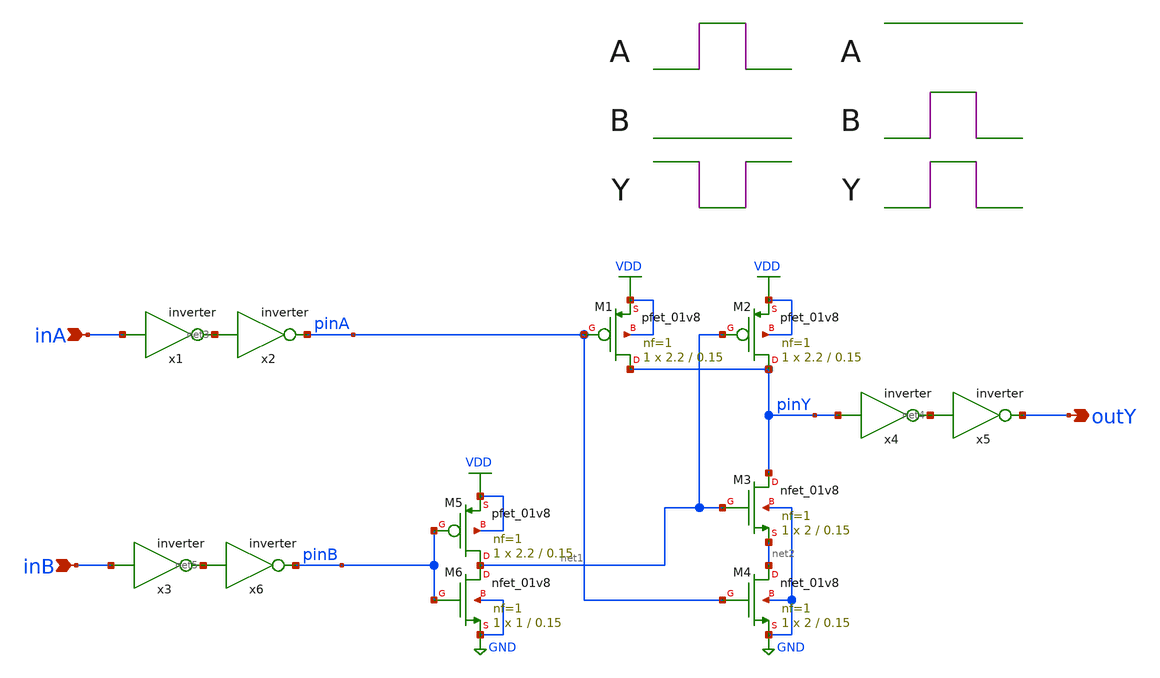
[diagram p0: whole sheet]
** sch_path: nandb_delay.sch
**.subckt nandb_delay inA outY inB
*.ipin inA
*.opin outY
*.ipin inB
x1 net3 inA inverter
x2 pinA net3 inverter
x4 net4 pinY inverter
x5 outY net4 inverter
x3 net5 inB inverter
x6 pinB net5 inverter
XM1 pinY pinA VDD VDD sky130_fd_pr__pfet_01v8 L=0.15 W=2.2 nf=1 ad='int((nf+1)/2) * W/nf * 0.29' as='int((nf+2)/2) * W/nf * 0.29'
+ pd='2*int((nf+1)/2) * (W/nf + 0.29)' ps='2*int((nf+2)/2) * (W/nf + 0.29)' nrd='0.29 / W' nrs='0.29 / W'
+ sa=0 sb=0 sd=0 mult=1 m=1
XM2 pinY net1 VDD VDD sky130_fd_pr__pfet_01v8 L=0.15 W=2.2 nf=1 ad='int((nf+1)/2) * W/nf * 0.29' as='int((nf+2)/2) * W/nf * 0.29'
+ pd='2*int((nf+1)/2) * (W/nf + 0.29)' ps='2*int((nf+2)/2) * (W/nf + 0.29)' nrd='0.29 / W' nrs='0.29 / W'
+ sa=0 sb=0 sd=0 mult=1 m=1
XM3 pinY net1 net2 GND sky130_fd_pr__nfet_01v8 L=0.15 W=2 nf=1 ad='int((nf+1)/2) * W/nf * 0.29' as='int((nf+2)/2) * W/nf * 0.29'
+ pd='2*int((nf+1)/2) * (W/nf + 0.29)' ps='2*int((nf+2)/2) * (W/nf + 0.29)' nrd='0.29 / W' nrs='0.29 / W'
+ sa=0 sb=0 sd=0 mult=1 m=1
XM4 net2 pinA GND GND sky130_fd_pr__nfet_01v8 L=0.15 W=2 nf=1 ad='int((nf+1)/2) * W/nf * 0.29' as='int((nf+2)/2) * W/nf * 0.29'
+ pd='2*int((nf+1)/2) * (W/nf + 0.29)' ps='2*int((nf+2)/2) * (W/nf + 0.29)' nrd='0.29 / W' nrs='0.29 / W'
+ sa=0 sb=0 sd=0 mult=1 m=1
XM5 net1 pinB VDD VDD sky130_fd_pr__pfet_01v8 L=0.15 W=2.2 nf=1 ad='int((nf+1)/2) * W/nf * 0.29' as='int((nf+2)/2) * W/nf * 0.29'
+ pd='2*int((nf+1)/2) * (W/nf + 0.29)' ps='2*int((nf+2)/2) * (W/nf + 0.29)' nrd='0.29 / W' nrs='0.29 / W'
+ sa=0 sb=0 sd=0 mult=1 m=1
XM6 net1 pinB GND GND sky130_fd_pr__nfet_01v8 L=0.15 W=1 nf=1 ad='int((nf+1)/2) * W/nf * 0.29' as='int((nf+2)/2) * W/nf * 0.29'
+ pd='2*int((nf+1)/2) * (W/nf + 0.29)' ps='2*int((nf+2)/2) * (W/nf + 0.29)' nrd='0.29 / W' nrs='0.29 / W'
+ sa=0 sb=0 sd=0 mult=1 m=1
**** begin user architecture code


VA inA 0 dc 0
VB inB 0 dc 0
VD VDD 0 dc 1.8
.control
alter @va[PULSE] [ 0 1.8 1n 40p 40p 1n 3n ]
alter @vb[PULSE] [ 0 0 1n 40p 40p 1n 3n ]
tran 10p 3n
meas tran  in1 FIND time WHEN v(pina)=0.9 RISE=1 > NUL
meas tran out1 FIND time WHEN v(piny)=0.9 FALL=1 > NUL
meas tran  in2 FIND time WHEN v(pina)=0.9 FALL=1 > NUL
meas tran out2 FIND time WHEN v(piny)=0.9 RISE=1 > NUL

let calc1 = out1 - in1
set delaynab1 = $&calc1
let calc2 = out2 - in2
set delaynab2 = $&calc2

alter @vb[PULSE] [ 0 1.8 1n 40p 40p 1n 3n ]
alter @va[PULSE] [ 1.8 1.8 1n 40p 40p 1n 3n ]
tran 10p 3n
meas tran  in5 FIND time WHEN v(pinb)=0.9 RISE=1 > NUL
meas tran out5 FIND time WHEN v(piny)=0.9 RISE=1 > NUL
meas tran  in6 FIND time WHEN v(pinb)=0.9 FALL=1 > NUL
meas tran out6 FIND time WHEN v(piny)=0.9 FALL=1 > NUL

let calc5 = out5 - in5
set delaynab5 = $&calc5
let calc6 = out6 - in6
set delaynab6 = $&calc6

let calc5 = out5 - in5
set delayna5 = $&calc5
let calc6 = out6 - in6
set delayna6 = $&calc6

echo '*** NANDB DELAY CASE 1 ***'
echo 'A(LH) when B(H) ='{$delaynab1}
echo 'A(HL) when B(H) ='{$delaynab2}

echo '*** NANDB DELAY CASE 2 ***'
echo 'B(LH) when A(H) ='{$delaynab5}
echo 'B(HL) when A(H) ='{$delaynab6}

.endc


** opencircuitdesign pdks install
.lib $::SKYWATER_MODELS/sky130.lib.spice tt


**** end user architecture code
**.ends

* expanding   symbol:  inverter.sym # of pins=2
** sym_path: inverter.sym
** sch_path: inverter.sch
.subckt inverter Y A
*.ipin A
*.opin Y
XM1 Y A VDD VDD sky130_fd_pr__pfet_01v8 L=0.15 W=2.2 nf=1 ad='int((nf+1)/2) * W/nf * 0.29' as='int((nf+2)/2) * W/nf * 0.29'
+ pd='2*int((nf+1)/2) * (W/nf + 0.29)' ps='2*int((nf+2)/2) * (W/nf + 0.29)' nrd='0.29 / W' nrs='0.29 / W'
+ sa=0 sb=0 sd=0 mult=1 m=1
XM2 Y A GND GND sky130_fd_pr__nfet_01v8 L=0.15 W=1 nf=1 ad='int((nf+1)/2) * W/nf * 0.29' as='int((nf+2)/2) * W/nf * 0.29'
+ pd='2*int((nf+1)/2) * (W/nf + 0.29)' ps='2*int((nf+2)/2) * (W/nf + 0.29)' nrd='0.29 / W' nrs='0.29 / W'
+ sa=0 sb=0 sd=0 mult=1 m=1
.ends

.GLOBAL VDD
.GLOBAL GND
.end
